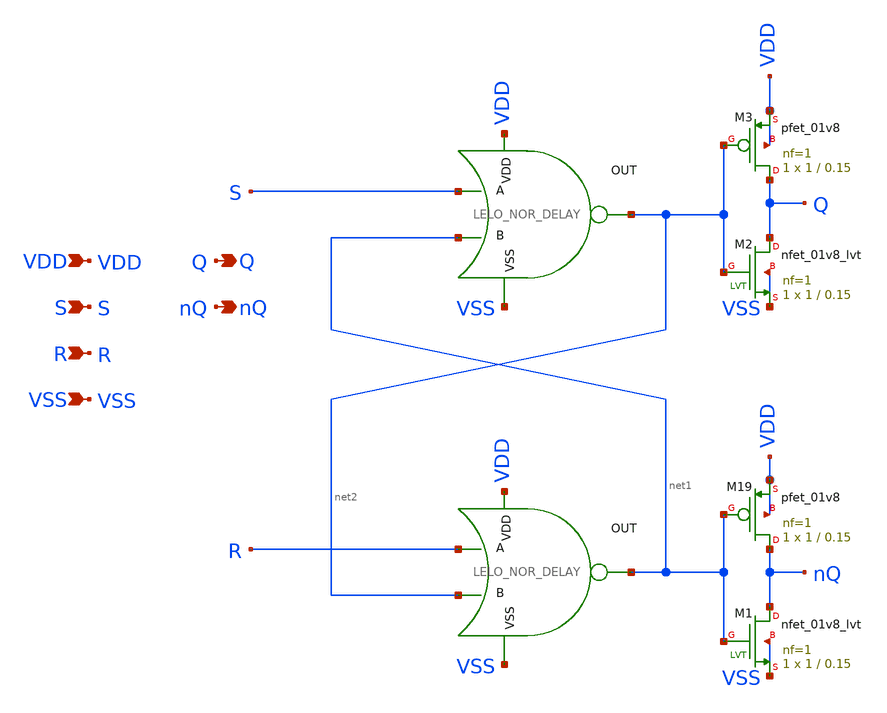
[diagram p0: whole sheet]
** sch_path: design/LELO_SVOD_SKY130A/SR_LATCH_DELAY.sch
**.subckt SR_LATCH_DELAY S R VSS VDD Q nQ
*.ipin S
*.ipin R
*.ipin VSS
*.ipin VDD
*.opin Q
*.opin nQ
XM3 Q net2 VDD VDD sky130_fd_pr__pfet_01v8 L=0.15 W=1 nf=1 ad='int((1 + 1)/2) * 1 / 1 * 0.29' as='int((1 + 2)/2) * 1 / 1 * 0.29'
+ pd='2*int((1 + 1)/2) * (1 / 1 + 0.29)' ps='2*int((1 + 2)/2) * (1 / 1 + 0.29)' nrd='0.29 / 1 ' nrs='0.29 / 1 '
+ sa=0 sb=0 sd=0 mult=1 m=1
XM19 nQ net1 VDD VDD sky130_fd_pr__pfet_01v8 L=0.15 W=1 nf=1 ad='int((1 + 1)/2) * 1 / 1 * 0.29' as='int((1 + 2)/2) * 1 / 1 * 0.29'
+ pd='2*int((1 + 1)/2) * (1 / 1 + 0.29)' ps='2*int((1 + 2)/2) * (1 / 1 + 0.29)' nrd='0.29 / 1 ' nrs='0.29 / 1 '
+ sa=0 sb=0 sd=0 mult=1 m=1
XM1 nQ net1 VSS VSS sky130_fd_pr__nfet_01v8_lvt L=0.15 W=1 nf=1 ad='int((1 + 1)/2) * 1 / 1 * 0.29' as='int((1 + 2)/2) * 1 / 1 * 0.29'
+ pd='2*int((1 + 1)/2) * (1 / 1 + 0.29)' ps='2*int((1 + 2)/2) * (1 / 1 + 0.29)' nrd='0.29 / 1 ' nrs='0.29 / 1 '
+ sa=0 sb=0 sd=0 mult=1 m=1
XM2 Q net2 VSS VSS sky130_fd_pr__nfet_01v8_lvt L=0.15 W=1 nf=1 ad='int((1 + 1)/2) * 1 / 1 * 0.29' as='int((1 + 2)/2) * 1 / 1 * 0.29'
+ pd='2*int((1 + 1)/2) * (1 / 1 + 0.29)' ps='2*int((1 + 2)/2) * (1 / 1 + 0.29)' nrd='0.29 / 1 ' nrs='0.29 / 1 '
+ sa=0 sb=0 sd=0 mult=1 m=1
x1 VDD net2 S net1 VSS LELO_NOR_DELAY
x2 VDD net1 R net2 VSS LELO_NOR_DELAY
**.ends

* expanding   symbol:  LELO_SVOD_SKY130A/LELO_NOR_DELAY.sym # of pins=5
** sym_path: design/LELO_SVOD_SKY130A/LELO_NOR_DELAY.sym
** sch_path: design/LELO_SVOD_SKY130A/LELO_NOR_DELAY.sch
.subckt LELO_NOR_DELAY VDD OUT A B VSS
*.ipin VDD
*.ipin VSS
*.opin OUT
*.ipin A
*.ipin B
XM3 OUT B net1 VDD sky130_fd_pr__pfet_01v8_lvt L=0.35 W=1 nf=1 ad='int((1 + 1)/2) * 1 / 1 * 0.29' as='int((1 + 2)/2) * 1 / 1 * 0.29'
+ pd='2*int((1 + 1)/2) * (1 / 1 + 0.29)' ps='2*int((1 + 2)/2) * (1 / 1 + 0.29)' nrd='0.29 / 1 ' nrs='0.29 / 1 '
+ sa=0 sb=0 sd=0 mult=1 m=1
XM1 OUT B VSS VSS sky130_fd_pr__nfet_01v8_lvt L=0.15 W=2 nf=1 ad='int((1 + 1)/2) * 2 / 1 * 0.29' as='int((1 + 2)/2) * 2 / 1 * 0.29'
+ pd='2*int((1 + 1)/2) * (2 / 1 + 0.29)' ps='2*int((1 + 2)/2) * (2 / 1 + 0.29)' nrd='0.29 / 2 ' nrs='0.29 / 2 '
+ sa=0 sb=0 sd=0 mult=1 m=1
XM2 OUT A VSS VSS sky130_fd_pr__nfet_01v8_lvt L=0.15 W=4 nf=1 ad='int((1 + 1)/2) * 4 / 1 * 0.29' as='int((1 + 2)/2) * 4 / 1 * 0.29'
+ pd='2*int((1 + 1)/2) * (4 / 1 + 0.29)' ps='2*int((1 + 2)/2) * (4 / 1 + 0.29)' nrd='0.29 / 4 ' nrs='0.29 / 4 '
+ sa=0 sb=0 sd=0 mult=1 m=1
XM4 net1 A VDD VDD sky130_fd_pr__pfet_01v8_lvt L=0.35 W=1 nf=1 ad='int((1 + 1)/2) * 1 / 1 * 0.29' as='int((1 + 2)/2) * 1 / 1 * 0.29'
+ pd='2*int((1 + 1)/2) * (1 / 1 + 0.29)' ps='2*int((1 + 2)/2) * (1 / 1 + 0.29)' nrd='0.29 / 1 ' nrs='0.29 / 1 '
+ sa=0 sb=0 sd=0 mult=1 m=1
.ends

.end
